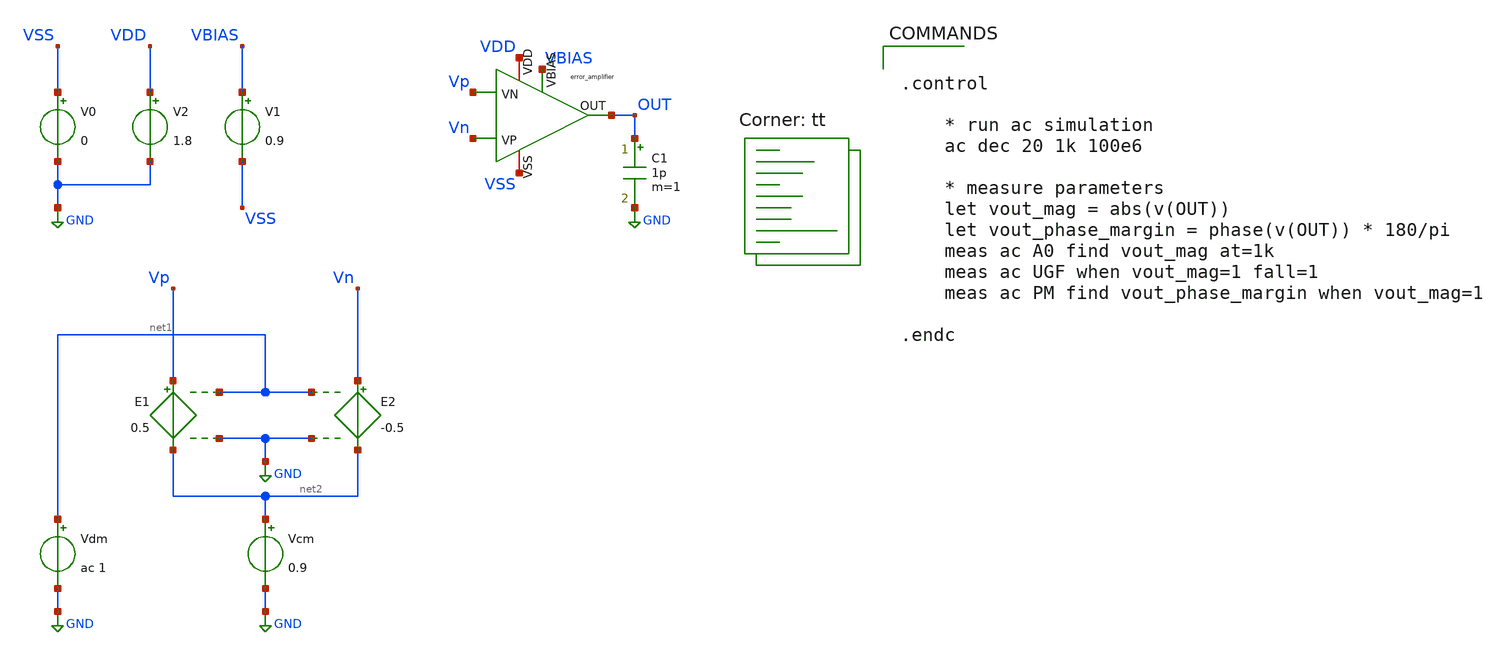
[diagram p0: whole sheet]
** sch_path: LDO_UVLO_Design/testbench/tb_error-amplifier/phase-margin.sch
**.subckt phase-margin
C1 OUT GND 1p m=1
V0 VSS GND 0
V2 VDD GND 1.8
E1 Vp net2 net1 GND 0.5
E2 Vn net2 net1 GND -0.5
Vdm net1 GND ac 1
Vcm net2 GND 0.9
x1 VDD VBIAS Vn Vp OUT VSS error_amplifier
V1 VBIAS VSS 0.9
**** begin user architecture code


.control

    * run ac simulation
    ac dec 20 1k 100e6

    * measure parameters
    let vout_mag = abs(v(OUT))
    let vout_phase_margin = phase(v(OUT)) * 180/pi
    meas ac A0 find vout_mag at=1k
    meas ac UGF when vout_mag=1 fall=1
    meas ac PM find vout_phase_margin when vout_mag=1

.endc


.lib $::SKYWATER_MODELS/sky130.lib.spice tt
**** end user architecture code
**.ends

* expanding   symbol:  ldo-sky130A-its/LDO_UVLO_Design/schematics/error_amplifier.sym # of pins=6
** sym_path: LDO_UVLO_Design/schematics/error_amplifier.sym
** sch_path: LDO_UVLO_Design/schematics/error_amplifier.sch
.subckt error_amplifier VDD VBIAS VP VN OUT VSS
*.iopin VDD
*.iopin VSS
*.ipin VBIAS
*.ipin VP
*.ipin VN
*.opin OUT
XM1 net2 net2 VSS VSS sky130_fd_pr__nfet_01v8 L=1.5 W=12 nf=1 ad='int((nf+1)/2) * W/nf * 0.29' as='int((nf+2)/2) * W/nf * 0.29'
+ pd='2*int((nf+1)/2) * (W/nf + 0.29)' ps='2*int((nf+2)/2) * (W/nf + 0.29)' nrd='0.29 / W' nrs='0.29 / W'
+ sa=0 sb=0 sd=0 mult=1 m=1
XM2 net1 net1 VSS VSS sky130_fd_pr__nfet_01v8 L=1.5 W=12 nf=1 ad='int((nf+1)/2) * W/nf * 0.29' as='int((nf+2)/2) * W/nf * 0.29'
+ pd='2*int((nf+1)/2) * (W/nf + 0.29)' ps='2*int((nf+2)/2) * (W/nf + 0.29)' nrd='0.29 / W' nrs='0.29 / W'
+ sa=0 sb=0 sd=0 mult=1 m=1
XM3 net2 VP net4 VDD sky130_fd_pr__pfet_01v8 L=1.5 W=12 nf=1 ad='int((nf+1)/2) * W/nf * 0.29' as='int((nf+2)/2) * W/nf * 0.29'
+ pd='2*int((nf+1)/2) * (W/nf + 0.29)' ps='2*int((nf+2)/2) * (W/nf + 0.29)' nrd='0.29 / W' nrs='0.29 / W'
+ sa=0 sb=0 sd=0 mult=1 m=1
XM4 net1 VN net4 VDD sky130_fd_pr__pfet_01v8 L=1.5 W=12 nf=1 ad='int((nf+1)/2) * W/nf * 0.29' as='int((nf+2)/2) * W/nf * 0.29'
+ pd='2*int((nf+1)/2) * (W/nf + 0.29)' ps='2*int((nf+2)/2) * (W/nf + 0.29)' nrd='0.29 / W' nrs='0.29 / W'
+ sa=0 sb=0 sd=0 mult=1 m=1
XM7 net3 net1 VSS VSS sky130_fd_pr__nfet_01v8 L=1.5 W=12 nf=1 ad='int((nf+1)/2) * W/nf * 0.29' as='int((nf+2)/2) * W/nf * 0.29'
+ pd='2*int((nf+1)/2) * (W/nf + 0.29)' ps='2*int((nf+2)/2) * (W/nf + 0.29)' nrd='0.29 / W' nrs='0.29 / W'
+ sa=0 sb=0 sd=0 mult=1 m=1
XM8 OUT net2 VSS VSS sky130_fd_pr__nfet_01v8 L=1.5 W=12 nf=1 ad='int((nf+1)/2) * W/nf * 0.29' as='int((nf+2)/2) * W/nf * 0.29'
+ pd='2*int((nf+1)/2) * (W/nf + 0.29)' ps='2*int((nf+2)/2) * (W/nf + 0.29)' nrd='0.29 / W' nrs='0.29 / W'
+ sa=0 sb=0 sd=0 mult=1 m=1
XM9 net3 net3 VDD VDD sky130_fd_pr__pfet_01v8 L=1.5 W=12 nf=1 ad='int((nf+1)/2) * W/nf * 0.29' as='int((nf+2)/2) * W/nf * 0.29'
+ pd='2*int((nf+1)/2) * (W/nf + 0.29)' ps='2*int((nf+2)/2) * (W/nf + 0.29)' nrd='0.29 / W' nrs='0.29 / W'
+ sa=0 sb=0 sd=0 mult=1 m=1
XM10 OUT net3 VDD VDD sky130_fd_pr__pfet_01v8 L=1.5 W=12 nf=1 ad='int((nf+1)/2) * W/nf * 0.29' as='int((nf+2)/2) * W/nf * 0.29'
+ pd='2*int((nf+1)/2) * (W/nf + 0.29)' ps='2*int((nf+2)/2) * (W/nf + 0.29)' nrd='0.29 / W' nrs='0.29 / W'
+ sa=0 sb=0 sd=0 mult=1 m=1
XM11 net4 VBIAS VDD VDD sky130_fd_pr__pfet_01v8 L=1.5 W=12 nf=1 ad='int((nf+1)/2) * W/nf * 0.29' as='int((nf+2)/2) * W/nf * 0.29'
+ pd='2*int((nf+1)/2) * (W/nf + 0.29)' ps='2*int((nf+2)/2) * (W/nf + 0.29)' nrd='0.29 / W' nrs='0.29 / W'
+ sa=0 sb=0 sd=0 mult=1 m=1
.ends

.GLOBAL GND
.end
